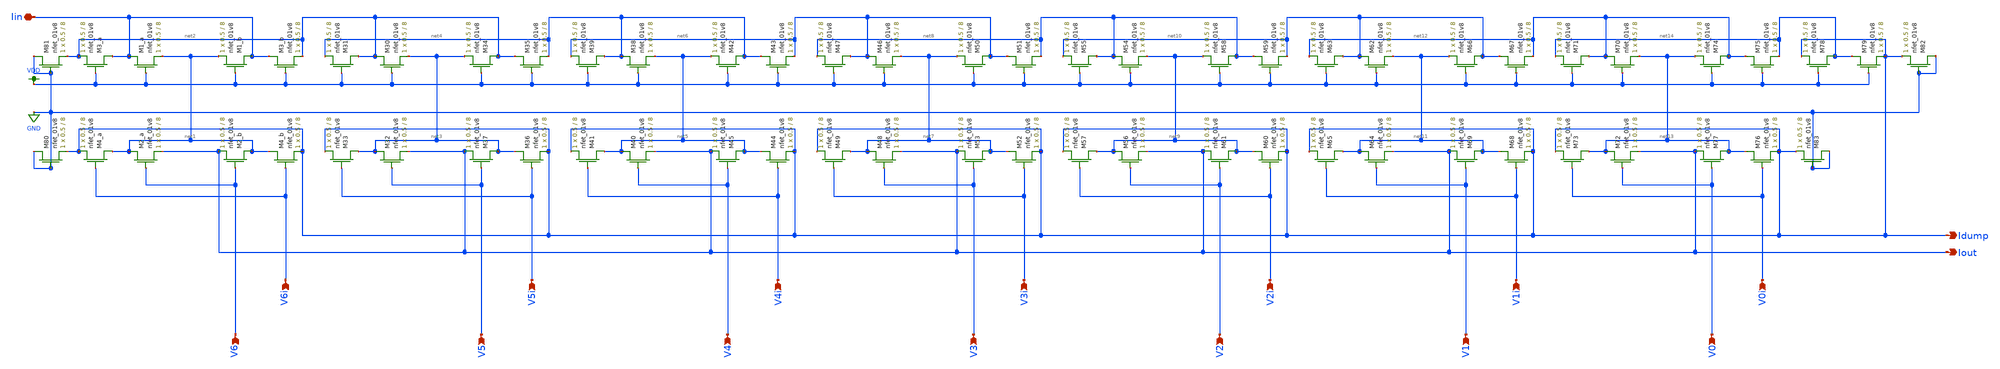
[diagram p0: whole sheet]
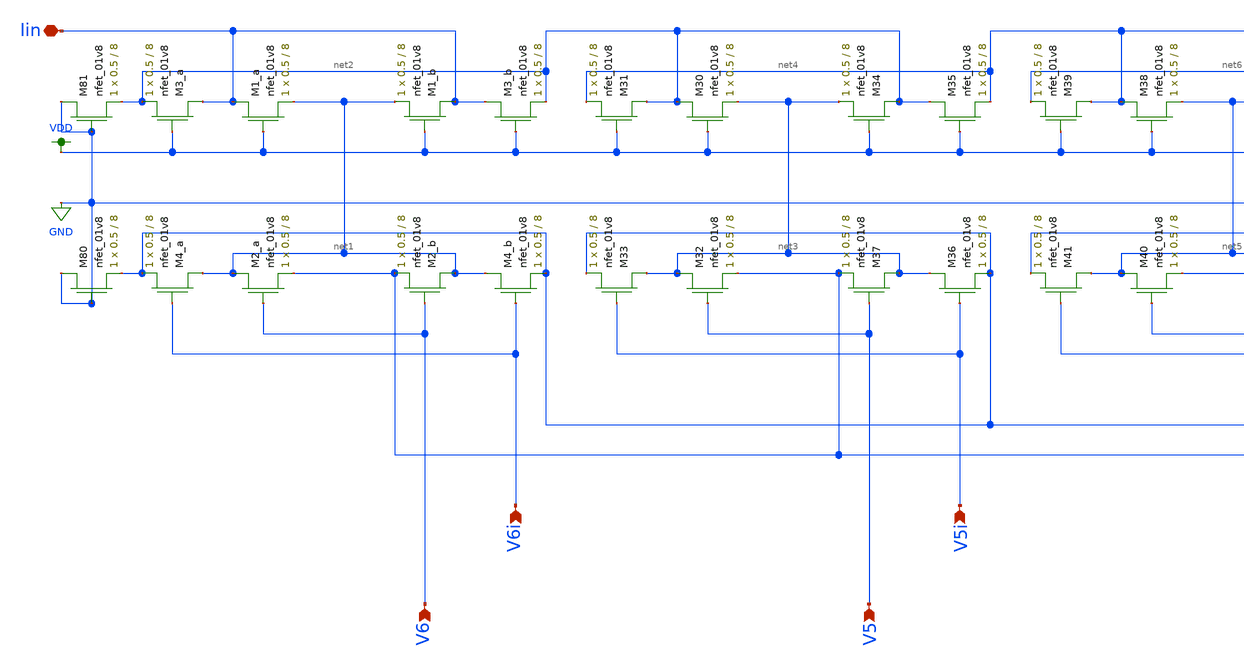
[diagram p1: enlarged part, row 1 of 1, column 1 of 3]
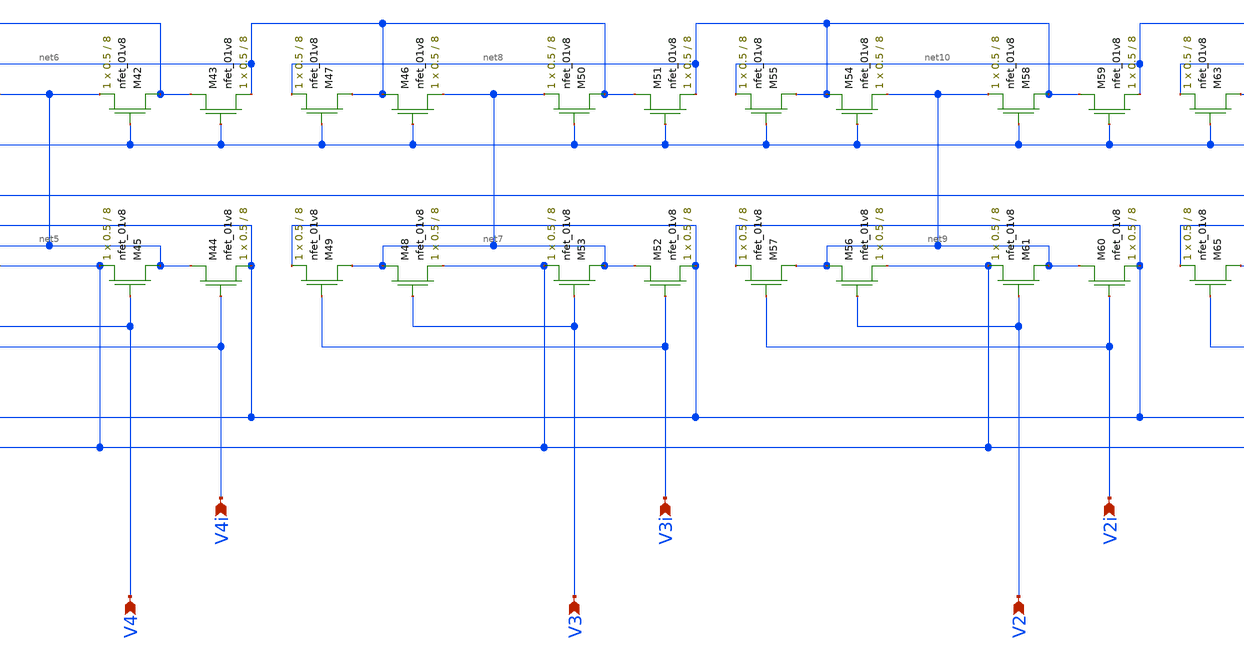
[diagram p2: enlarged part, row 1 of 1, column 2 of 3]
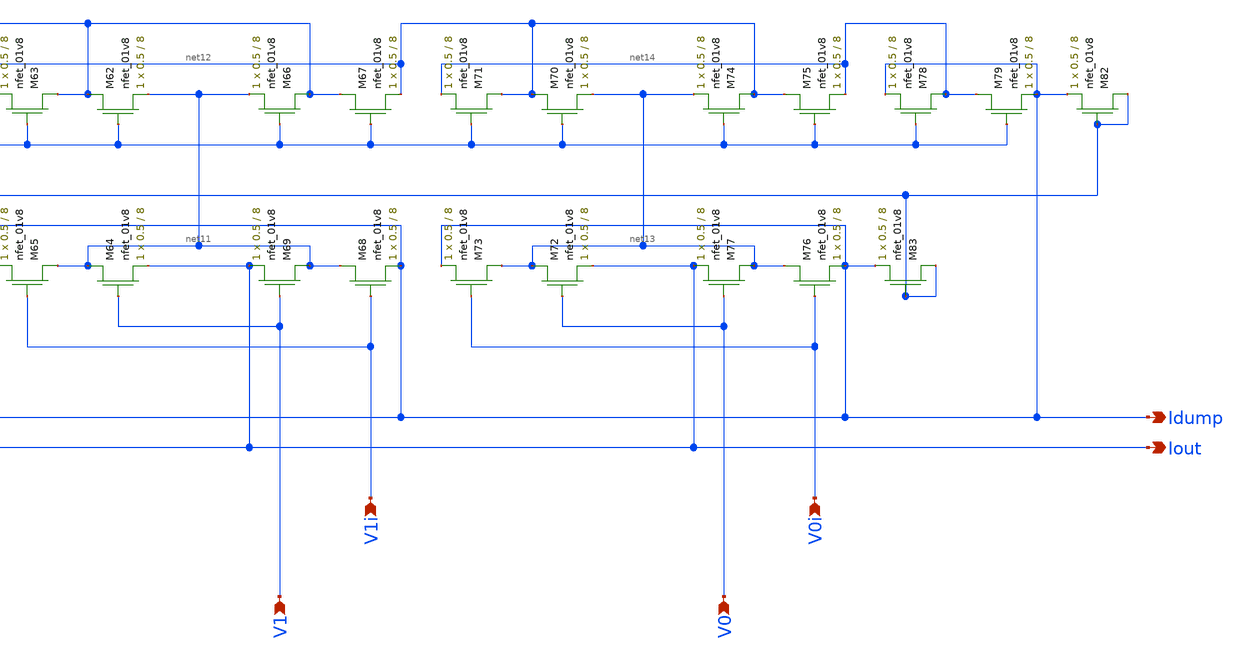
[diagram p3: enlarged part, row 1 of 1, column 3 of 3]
** sch_path: xschem/old_files/ladder.sch
**.subckt ladder Iin Idump Iout V6 V5 V4 V3 V2 V1 V0 V6i V5i V4i V3i V2i V1i V0i
*.iopin Iin
*.opin Idump
*.opin Iout
*.ipin V6
*.ipin V5
*.ipin V4
*.ipin V3
*.ipin V2
*.ipin V1
*.ipin V0
*.ipin V6i
*.ipin V5i
*.ipin V4i
*.ipin V3i
*.ipin V2i
*.ipin V1i
*.ipin V0i
XM1_a Iin VDD net1 GND sky130_fd_pr__nfet_01v8 L=8 W=0.5 nf=1 ad='int((nf+1)/2) * W/nf * 0.29' as='int((nf+2)/2) * W/nf * 0.29'
+ pd='2*int((nf+1)/2) * (W/nf + 0.29)' ps='2*int((nf+2)/2) * (W/nf + 0.29)' nrd='0.29 / W' nrs='0.29 / W'
+ sa=0 sb=0 sd=0 mult=1 m=1
XM3_a Iin VDD net2 GND sky130_fd_pr__nfet_01v8 L=8 W=0.5 nf=1 ad='int((nf+1)/2) * W/nf * 0.29' as='int((nf+2)/2) * W/nf * 0.29'
+ pd='2*int((nf+1)/2) * (W/nf + 0.29)' ps='2*int((nf+2)/2) * (W/nf + 0.29)' nrd='0.29 / W' nrs='0.29 / W'
+ sa=0 sb=0 sd=0 mult=1 m=1
XM2_a net1 V6 Iout GND sky130_fd_pr__nfet_01v8 L=8 W=0.5 nf=1 ad='int((nf+1)/2) * W/nf * 0.29' as='int((nf+2)/2) * W/nf * 0.29'
+ pd='2*int((nf+1)/2) * (W/nf + 0.29)' ps='2*int((nf+2)/2) * (W/nf + 0.29)' nrd='0.29 / W' nrs='0.29 / W'
+ sa=0 sb=0 sd=0 mult=1 m=1
XM4_a net1 V6i Idump GND sky130_fd_pr__nfet_01v8 L=8 W=0.5 nf=1 ad='int((nf+1)/2) * W/nf * 0.29' as='int((nf+2)/2) * W/nf * 0.29'
+ pd='2*int((nf+1)/2) * (W/nf + 0.29)' ps='2*int((nf+2)/2) * (W/nf + 0.29)' nrd='0.29 / W' nrs='0.29 / W'
+ sa=0 sb=0 sd=0 mult=1 m=1
XM1_b Iin VDD net1 GND sky130_fd_pr__nfet_01v8 L=8 W=0.5 nf=1 ad='int((nf+1)/2) * W/nf * 0.29' as='int((nf+2)/2) * W/nf * 0.29'
+ pd='2*int((nf+1)/2) * (W/nf + 0.29)' ps='2*int((nf+2)/2) * (W/nf + 0.29)' nrd='0.29 / W' nrs='0.29 / W'
+ sa=0 sb=0 sd=0 mult=1 m=1
XM3_b Iin VDD net2 GND sky130_fd_pr__nfet_01v8 L=8 W=0.5 nf=1 ad='int((nf+1)/2) * W/nf * 0.29' as='int((nf+2)/2) * W/nf * 0.29'
+ pd='2*int((nf+1)/2) * (W/nf + 0.29)' ps='2*int((nf+2)/2) * (W/nf + 0.29)' nrd='0.29 / W' nrs='0.29 / W'
+ sa=0 sb=0 sd=0 mult=1 m=1
XM4_b net1 V6i Idump GND sky130_fd_pr__nfet_01v8 L=8 W=0.5 nf=1 ad='int((nf+1)/2) * W/nf * 0.29' as='int((nf+2)/2) * W/nf * 0.29'
+ pd='2*int((nf+1)/2) * (W/nf + 0.29)' ps='2*int((nf+2)/2) * (W/nf + 0.29)' nrd='0.29 / W' nrs='0.29 / W'
+ sa=0 sb=0 sd=0 mult=1 m=1
XM2_b net1 V6 Iout GND sky130_fd_pr__nfet_01v8 L=8 W=0.5 nf=1 ad='int((nf+1)/2) * W/nf * 0.29' as='int((nf+2)/2) * W/nf * 0.29'
+ pd='2*int((nf+1)/2) * (W/nf + 0.29)' ps='2*int((nf+2)/2) * (W/nf + 0.29)' nrd='0.29 / W' nrs='0.29 / W'
+ sa=0 sb=0 sd=0 mult=1 m=1
XM30 net2 VDD net3 GND sky130_fd_pr__nfet_01v8 L=8 W=0.5 nf=1 ad='int((nf+1)/2) * W/nf * 0.29' as='int((nf+2)/2) * W/nf * 0.29'
+ pd='2*int((nf+1)/2) * (W/nf + 0.29)' ps='2*int((nf+2)/2) * (W/nf + 0.29)' nrd='0.29 / W' nrs='0.29 / W'
+ sa=0 sb=0 sd=0 mult=1 m=1
XM31 net2 VDD net4 GND sky130_fd_pr__nfet_01v8 L=8 W=0.5 nf=1 ad='int((nf+1)/2) * W/nf * 0.29' as='int((nf+2)/2) * W/nf * 0.29'
+ pd='2*int((nf+1)/2) * (W/nf + 0.29)' ps='2*int((nf+2)/2) * (W/nf + 0.29)' nrd='0.29 / W' nrs='0.29 / W'
+ sa=0 sb=0 sd=0 mult=1 m=1
XM32 net3 V5 Iout GND sky130_fd_pr__nfet_01v8 L=8 W=0.5 nf=1 ad='int((nf+1)/2) * W/nf * 0.29' as='int((nf+2)/2) * W/nf * 0.29'
+ pd='2*int((nf+1)/2) * (W/nf + 0.29)' ps='2*int((nf+2)/2) * (W/nf + 0.29)' nrd='0.29 / W' nrs='0.29 / W'
+ sa=0 sb=0 sd=0 mult=1 m=1
XM33 net3 V5i Idump GND sky130_fd_pr__nfet_01v8 L=8 W=0.5 nf=1 ad='int((nf+1)/2) * W/nf * 0.29' as='int((nf+2)/2) * W/nf * 0.29'
+ pd='2*int((nf+1)/2) * (W/nf + 0.29)' ps='2*int((nf+2)/2) * (W/nf + 0.29)' nrd='0.29 / W' nrs='0.29 / W'
+ sa=0 sb=0 sd=0 mult=1 m=1
XM34 net2 VDD net3 GND sky130_fd_pr__nfet_01v8 L=8 W=0.5 nf=1 ad='int((nf+1)/2) * W/nf * 0.29' as='int((nf+2)/2) * W/nf * 0.29'
+ pd='2*int((nf+1)/2) * (W/nf + 0.29)' ps='2*int((nf+2)/2) * (W/nf + 0.29)' nrd='0.29 / W' nrs='0.29 / W'
+ sa=0 sb=0 sd=0 mult=1 m=1
XM35 net2 VDD net4 GND sky130_fd_pr__nfet_01v8 L=8 W=0.5 nf=1 ad='int((nf+1)/2) * W/nf * 0.29' as='int((nf+2)/2) * W/nf * 0.29'
+ pd='2*int((nf+1)/2) * (W/nf + 0.29)' ps='2*int((nf+2)/2) * (W/nf + 0.29)' nrd='0.29 / W' nrs='0.29 / W'
+ sa=0 sb=0 sd=0 mult=1 m=1
XM36 net3 V5i Idump GND sky130_fd_pr__nfet_01v8 L=8 W=0.5 nf=1 ad='int((nf+1)/2) * W/nf * 0.29' as='int((nf+2)/2) * W/nf * 0.29'
+ pd='2*int((nf+1)/2) * (W/nf + 0.29)' ps='2*int((nf+2)/2) * (W/nf + 0.29)' nrd='0.29 / W' nrs='0.29 / W'
+ sa=0 sb=0 sd=0 mult=1 m=1
XM37 net3 V5 Iout GND sky130_fd_pr__nfet_01v8 L=8 W=0.5 nf=1 ad='int((nf+1)/2) * W/nf * 0.29' as='int((nf+2)/2) * W/nf * 0.29'
+ pd='2*int((nf+1)/2) * (W/nf + 0.29)' ps='2*int((nf+2)/2) * (W/nf + 0.29)' nrd='0.29 / W' nrs='0.29 / W'
+ sa=0 sb=0 sd=0 mult=1 m=1
XM38 net4 VDD net5 GND sky130_fd_pr__nfet_01v8 L=8 W=0.5 nf=1 ad='int((nf+1)/2) * W/nf * 0.29' as='int((nf+2)/2) * W/nf * 0.29'
+ pd='2*int((nf+1)/2) * (W/nf + 0.29)' ps='2*int((nf+2)/2) * (W/nf + 0.29)' nrd='0.29 / W' nrs='0.29 / W'
+ sa=0 sb=0 sd=0 mult=1 m=1
XM39 net4 VDD net6 GND sky130_fd_pr__nfet_01v8 L=8 W=0.5 nf=1 ad='int((nf+1)/2) * W/nf * 0.29' as='int((nf+2)/2) * W/nf * 0.29'
+ pd='2*int((nf+1)/2) * (W/nf + 0.29)' ps='2*int((nf+2)/2) * (W/nf + 0.29)' nrd='0.29 / W' nrs='0.29 / W'
+ sa=0 sb=0 sd=0 mult=1 m=1
XM40 net5 V4 Iout GND sky130_fd_pr__nfet_01v8 L=8 W=0.5 nf=1 ad='int((nf+1)/2) * W/nf * 0.29' as='int((nf+2)/2) * W/nf * 0.29'
+ pd='2*int((nf+1)/2) * (W/nf + 0.29)' ps='2*int((nf+2)/2) * (W/nf + 0.29)' nrd='0.29 / W' nrs='0.29 / W'
+ sa=0 sb=0 sd=0 mult=1 m=1
XM41 net5 V4i Idump GND sky130_fd_pr__nfet_01v8 L=8 W=0.5 nf=1 ad='int((nf+1)/2) * W/nf * 0.29' as='int((nf+2)/2) * W/nf * 0.29'
+ pd='2*int((nf+1)/2) * (W/nf + 0.29)' ps='2*int((nf+2)/2) * (W/nf + 0.29)' nrd='0.29 / W' nrs='0.29 / W'
+ sa=0 sb=0 sd=0 mult=1 m=1
XM42 net4 VDD net5 GND sky130_fd_pr__nfet_01v8 L=8 W=0.5 nf=1 ad='int((nf+1)/2) * W/nf * 0.29' as='int((nf+2)/2) * W/nf * 0.29'
+ pd='2*int((nf+1)/2) * (W/nf + 0.29)' ps='2*int((nf+2)/2) * (W/nf + 0.29)' nrd='0.29 / W' nrs='0.29 / W'
+ sa=0 sb=0 sd=0 mult=1 m=1
XM43 net4 VDD net6 GND sky130_fd_pr__nfet_01v8 L=8 W=0.5 nf=1 ad='int((nf+1)/2) * W/nf * 0.29' as='int((nf+2)/2) * W/nf * 0.29'
+ pd='2*int((nf+1)/2) * (W/nf + 0.29)' ps='2*int((nf+2)/2) * (W/nf + 0.29)' nrd='0.29 / W' nrs='0.29 / W'
+ sa=0 sb=0 sd=0 mult=1 m=1
XM44 net5 V4i Idump GND sky130_fd_pr__nfet_01v8 L=8 W=0.5 nf=1 ad='int((nf+1)/2) * W/nf * 0.29' as='int((nf+2)/2) * W/nf * 0.29'
+ pd='2*int((nf+1)/2) * (W/nf + 0.29)' ps='2*int((nf+2)/2) * (W/nf + 0.29)' nrd='0.29 / W' nrs='0.29 / W'
+ sa=0 sb=0 sd=0 mult=1 m=1
XM45 net5 V4 Iout GND sky130_fd_pr__nfet_01v8 L=8 W=0.5 nf=1 ad='int((nf+1)/2) * W/nf * 0.29' as='int((nf+2)/2) * W/nf * 0.29'
+ pd='2*int((nf+1)/2) * (W/nf + 0.29)' ps='2*int((nf+2)/2) * (W/nf + 0.29)' nrd='0.29 / W' nrs='0.29 / W'
+ sa=0 sb=0 sd=0 mult=1 m=1
XM46 net6 VDD net7 GND sky130_fd_pr__nfet_01v8 L=8 W=0.5 nf=1 ad='int((nf+1)/2) * W/nf * 0.29' as='int((nf+2)/2) * W/nf * 0.29'
+ pd='2*int((nf+1)/2) * (W/nf + 0.29)' ps='2*int((nf+2)/2) * (W/nf + 0.29)' nrd='0.29 / W' nrs='0.29 / W'
+ sa=0 sb=0 sd=0 mult=1 m=1
XM47 net6 VDD net8 GND sky130_fd_pr__nfet_01v8 L=8 W=0.5 nf=1 ad='int((nf+1)/2) * W/nf * 0.29' as='int((nf+2)/2) * W/nf * 0.29'
+ pd='2*int((nf+1)/2) * (W/nf + 0.29)' ps='2*int((nf+2)/2) * (W/nf + 0.29)' nrd='0.29 / W' nrs='0.29 / W'
+ sa=0 sb=0 sd=0 mult=1 m=1
XM48 net7 V3 Iout GND sky130_fd_pr__nfet_01v8 L=8 W=0.5 nf=1 ad='int((nf+1)/2) * W/nf * 0.29' as='int((nf+2)/2) * W/nf * 0.29'
+ pd='2*int((nf+1)/2) * (W/nf + 0.29)' ps='2*int((nf+2)/2) * (W/nf + 0.29)' nrd='0.29 / W' nrs='0.29 / W'
+ sa=0 sb=0 sd=0 mult=1 m=1
XM49 net7 V3i Idump GND sky130_fd_pr__nfet_01v8 L=8 W=0.5 nf=1 ad='int((nf+1)/2) * W/nf * 0.29' as='int((nf+2)/2) * W/nf * 0.29'
+ pd='2*int((nf+1)/2) * (W/nf + 0.29)' ps='2*int((nf+2)/2) * (W/nf + 0.29)' nrd='0.29 / W' nrs='0.29 / W'
+ sa=0 sb=0 sd=0 mult=1 m=1
XM50 net6 VDD net7 GND sky130_fd_pr__nfet_01v8 L=8 W=0.5 nf=1 ad='int((nf+1)/2) * W/nf * 0.29' as='int((nf+2)/2) * W/nf * 0.29'
+ pd='2*int((nf+1)/2) * (W/nf + 0.29)' ps='2*int((nf+2)/2) * (W/nf + 0.29)' nrd='0.29 / W' nrs='0.29 / W'
+ sa=0 sb=0 sd=0 mult=1 m=1
XM51 net6 VDD net8 GND sky130_fd_pr__nfet_01v8 L=8 W=0.5 nf=1 ad='int((nf+1)/2) * W/nf * 0.29' as='int((nf+2)/2) * W/nf * 0.29'
+ pd='2*int((nf+1)/2) * (W/nf + 0.29)' ps='2*int((nf+2)/2) * (W/nf + 0.29)' nrd='0.29 / W' nrs='0.29 / W'
+ sa=0 sb=0 sd=0 mult=1 m=1
XM52 net7 V3i Idump GND sky130_fd_pr__nfet_01v8 L=8 W=0.5 nf=1 ad='int((nf+1)/2) * W/nf * 0.29' as='int((nf+2)/2) * W/nf * 0.29'
+ pd='2*int((nf+1)/2) * (W/nf + 0.29)' ps='2*int((nf+2)/2) * (W/nf + 0.29)' nrd='0.29 / W' nrs='0.29 / W'
+ sa=0 sb=0 sd=0 mult=1 m=1
XM53 net7 V3 Iout GND sky130_fd_pr__nfet_01v8 L=8 W=0.5 nf=1 ad='int((nf+1)/2) * W/nf * 0.29' as='int((nf+2)/2) * W/nf * 0.29'
+ pd='2*int((nf+1)/2) * (W/nf + 0.29)' ps='2*int((nf+2)/2) * (W/nf + 0.29)' nrd='0.29 / W' nrs='0.29 / W'
+ sa=0 sb=0 sd=0 mult=1 m=1
XM54 net8 VDD net9 GND sky130_fd_pr__nfet_01v8 L=8 W=0.5 nf=1 ad='int((nf+1)/2) * W/nf * 0.29' as='int((nf+2)/2) * W/nf * 0.29'
+ pd='2*int((nf+1)/2) * (W/nf + 0.29)' ps='2*int((nf+2)/2) * (W/nf + 0.29)' nrd='0.29 / W' nrs='0.29 / W'
+ sa=0 sb=0 sd=0 mult=1 m=1
XM55 net8 VDD net10 GND sky130_fd_pr__nfet_01v8 L=8 W=0.5 nf=1 ad='int((nf+1)/2) * W/nf * 0.29' as='int((nf+2)/2) * W/nf * 0.29'
+ pd='2*int((nf+1)/2) * (W/nf + 0.29)' ps='2*int((nf+2)/2) * (W/nf + 0.29)' nrd='0.29 / W' nrs='0.29 / W'
+ sa=0 sb=0 sd=0 mult=1 m=1
XM56 net9 V2 Iout GND sky130_fd_pr__nfet_01v8 L=8 W=0.5 nf=1 ad='int((nf+1)/2) * W/nf * 0.29' as='int((nf+2)/2) * W/nf * 0.29'
+ pd='2*int((nf+1)/2) * (W/nf + 0.29)' ps='2*int((nf+2)/2) * (W/nf + 0.29)' nrd='0.29 / W' nrs='0.29 / W'
+ sa=0 sb=0 sd=0 mult=1 m=1
XM57 net9 V2i Idump GND sky130_fd_pr__nfet_01v8 L=8 W=0.5 nf=1 ad='int((nf+1)/2) * W/nf * 0.29' as='int((nf+2)/2) * W/nf * 0.29'
+ pd='2*int((nf+1)/2) * (W/nf + 0.29)' ps='2*int((nf+2)/2) * (W/nf + 0.29)' nrd='0.29 / W' nrs='0.29 / W'
+ sa=0 sb=0 sd=0 mult=1 m=1
XM58 net8 VDD net9 GND sky130_fd_pr__nfet_01v8 L=8 W=0.5 nf=1 ad='int((nf+1)/2) * W/nf * 0.29' as='int((nf+2)/2) * W/nf * 0.29'
+ pd='2*int((nf+1)/2) * (W/nf + 0.29)' ps='2*int((nf+2)/2) * (W/nf + 0.29)' nrd='0.29 / W' nrs='0.29 / W'
+ sa=0 sb=0 sd=0 mult=1 m=1
XM59 net8 VDD net10 GND sky130_fd_pr__nfet_01v8 L=8 W=0.5 nf=1 ad='int((nf+1)/2) * W/nf * 0.29' as='int((nf+2)/2) * W/nf * 0.29'
+ pd='2*int((nf+1)/2) * (W/nf + 0.29)' ps='2*int((nf+2)/2) * (W/nf + 0.29)' nrd='0.29 / W' nrs='0.29 / W'
+ sa=0 sb=0 sd=0 mult=1 m=1
XM60 net9 V2i Idump GND sky130_fd_pr__nfet_01v8 L=8 W=0.5 nf=1 ad='int((nf+1)/2) * W/nf * 0.29' as='int((nf+2)/2) * W/nf * 0.29'
+ pd='2*int((nf+1)/2) * (W/nf + 0.29)' ps='2*int((nf+2)/2) * (W/nf + 0.29)' nrd='0.29 / W' nrs='0.29 / W'
+ sa=0 sb=0 sd=0 mult=1 m=1
XM61 net9 V2 Iout GND sky130_fd_pr__nfet_01v8 L=8 W=0.5 nf=1 ad='int((nf+1)/2) * W/nf * 0.29' as='int((nf+2)/2) * W/nf * 0.29'
+ pd='2*int((nf+1)/2) * (W/nf + 0.29)' ps='2*int((nf+2)/2) * (W/nf + 0.29)' nrd='0.29 / W' nrs='0.29 / W'
+ sa=0 sb=0 sd=0 mult=1 m=1
XM62 net10 VDD net11 GND sky130_fd_pr__nfet_01v8 L=8 W=0.5 nf=1 ad='int((nf+1)/2) * W/nf * 0.29' as='int((nf+2)/2) * W/nf * 0.29'
+ pd='2*int((nf+1)/2) * (W/nf + 0.29)' ps='2*int((nf+2)/2) * (W/nf + 0.29)' nrd='0.29 / W' nrs='0.29 / W'
+ sa=0 sb=0 sd=0 mult=1 m=1
XM63 net10 VDD net12 GND sky130_fd_pr__nfet_01v8 L=8 W=0.5 nf=1 ad='int((nf+1)/2) * W/nf * 0.29' as='int((nf+2)/2) * W/nf * 0.29'
+ pd='2*int((nf+1)/2) * (W/nf + 0.29)' ps='2*int((nf+2)/2) * (W/nf + 0.29)' nrd='0.29 / W' nrs='0.29 / W'
+ sa=0 sb=0 sd=0 mult=1 m=1
XM64 net11 V1 Iout GND sky130_fd_pr__nfet_01v8 L=8 W=0.5 nf=1 ad='int((nf+1)/2) * W/nf * 0.29' as='int((nf+2)/2) * W/nf * 0.29'
+ pd='2*int((nf+1)/2) * (W/nf + 0.29)' ps='2*int((nf+2)/2) * (W/nf + 0.29)' nrd='0.29 / W' nrs='0.29 / W'
+ sa=0 sb=0 sd=0 mult=1 m=1
XM65 net11 V1i Idump GND sky130_fd_pr__nfet_01v8 L=8 W=0.5 nf=1 ad='int((nf+1)/2) * W/nf * 0.29' as='int((nf+2)/2) * W/nf * 0.29'
+ pd='2*int((nf+1)/2) * (W/nf + 0.29)' ps='2*int((nf+2)/2) * (W/nf + 0.29)' nrd='0.29 / W' nrs='0.29 / W'
+ sa=0 sb=0 sd=0 mult=1 m=1
XM66 net10 VDD net11 GND sky130_fd_pr__nfet_01v8 L=8 W=0.5 nf=1 ad='int((nf+1)/2) * W/nf * 0.29' as='int((nf+2)/2) * W/nf * 0.29'
+ pd='2*int((nf+1)/2) * (W/nf + 0.29)' ps='2*int((nf+2)/2) * (W/nf + 0.29)' nrd='0.29 / W' nrs='0.29 / W'
+ sa=0 sb=0 sd=0 mult=1 m=1
XM67 net10 VDD net12 GND sky130_fd_pr__nfet_01v8 L=8 W=0.5 nf=1 ad='int((nf+1)/2) * W/nf * 0.29' as='int((nf+2)/2) * W/nf * 0.29'
+ pd='2*int((nf+1)/2) * (W/nf + 0.29)' ps='2*int((nf+2)/2) * (W/nf + 0.29)' nrd='0.29 / W' nrs='0.29 / W'
+ sa=0 sb=0 sd=0 mult=1 m=1
XM68 net11 V1i Idump GND sky130_fd_pr__nfet_01v8 L=8 W=0.5 nf=1 ad='int((nf+1)/2) * W/nf * 0.29' as='int((nf+2)/2) * W/nf * 0.29'
+ pd='2*int((nf+1)/2) * (W/nf + 0.29)' ps='2*int((nf+2)/2) * (W/nf + 0.29)' nrd='0.29 / W' nrs='0.29 / W'
+ sa=0 sb=0 sd=0 mult=1 m=1
XM69 net11 V1 Iout GND sky130_fd_pr__nfet_01v8 L=8 W=0.5 nf=1 ad='int((nf+1)/2) * W/nf * 0.29' as='int((nf+2)/2) * W/nf * 0.29'
+ pd='2*int((nf+1)/2) * (W/nf + 0.29)' ps='2*int((nf+2)/2) * (W/nf + 0.29)' nrd='0.29 / W' nrs='0.29 / W'
+ sa=0 sb=0 sd=0 mult=1 m=1
XM70 net12 VDD net13 GND sky130_fd_pr__nfet_01v8 L=8 W=0.5 nf=1 ad='int((nf+1)/2) * W/nf * 0.29' as='int((nf+2)/2) * W/nf * 0.29'
+ pd='2*int((nf+1)/2) * (W/nf + 0.29)' ps='2*int((nf+2)/2) * (W/nf + 0.29)' nrd='0.29 / W' nrs='0.29 / W'
+ sa=0 sb=0 sd=0 mult=1 m=1
XM71 net12 VDD net14 GND sky130_fd_pr__nfet_01v8 L=8 W=0.5 nf=1 ad='int((nf+1)/2) * W/nf * 0.29' as='int((nf+2)/2) * W/nf * 0.29'
+ pd='2*int((nf+1)/2) * (W/nf + 0.29)' ps='2*int((nf+2)/2) * (W/nf + 0.29)' nrd='0.29 / W' nrs='0.29 / W'
+ sa=0 sb=0 sd=0 mult=1 m=1
XM72 net13 V0 Iout GND sky130_fd_pr__nfet_01v8 L=8 W=0.5 nf=1 ad='int((nf+1)/2) * W/nf * 0.29' as='int((nf+2)/2) * W/nf * 0.29'
+ pd='2*int((nf+1)/2) * (W/nf + 0.29)' ps='2*int((nf+2)/2) * (W/nf + 0.29)' nrd='0.29 / W' nrs='0.29 / W'
+ sa=0 sb=0 sd=0 mult=1 m=1
XM73 net13 V0i Idump GND sky130_fd_pr__nfet_01v8 L=8 W=0.5 nf=1 ad='int((nf+1)/2) * W/nf * 0.29' as='int((nf+2)/2) * W/nf * 0.29'
+ pd='2*int((nf+1)/2) * (W/nf + 0.29)' ps='2*int((nf+2)/2) * (W/nf + 0.29)' nrd='0.29 / W' nrs='0.29 / W'
+ sa=0 sb=0 sd=0 mult=1 m=1
XM74 net12 VDD net13 GND sky130_fd_pr__nfet_01v8 L=8 W=0.5 nf=1 ad='int((nf+1)/2) * W/nf * 0.29' as='int((nf+2)/2) * W/nf * 0.29'
+ pd='2*int((nf+1)/2) * (W/nf + 0.29)' ps='2*int((nf+2)/2) * (W/nf + 0.29)' nrd='0.29 / W' nrs='0.29 / W'
+ sa=0 sb=0 sd=0 mult=1 m=1
XM75 net12 VDD net14 GND sky130_fd_pr__nfet_01v8 L=8 W=0.5 nf=1 ad='int((nf+1)/2) * W/nf * 0.29' as='int((nf+2)/2) * W/nf * 0.29'
+ pd='2*int((nf+1)/2) * (W/nf + 0.29)' ps='2*int((nf+2)/2) * (W/nf + 0.29)' nrd='0.29 / W' nrs='0.29 / W'
+ sa=0 sb=0 sd=0 mult=1 m=1
XM76 net13 V0i Idump GND sky130_fd_pr__nfet_01v8 L=8 W=0.5 nf=1 ad='int((nf+1)/2) * W/nf * 0.29' as='int((nf+2)/2) * W/nf * 0.29'
+ pd='2*int((nf+1)/2) * (W/nf + 0.29)' ps='2*int((nf+2)/2) * (W/nf + 0.29)' nrd='0.29 / W' nrs='0.29 / W'
+ sa=0 sb=0 sd=0 mult=1 m=1
XM77 net13 V0 Iout GND sky130_fd_pr__nfet_01v8 L=8 W=0.5 nf=1 ad='int((nf+1)/2) * W/nf * 0.29' as='int((nf+2)/2) * W/nf * 0.29'
+ pd='2*int((nf+1)/2) * (W/nf + 0.29)' ps='2*int((nf+2)/2) * (W/nf + 0.29)' nrd='0.29 / W' nrs='0.29 / W'
+ sa=0 sb=0 sd=0 mult=1 m=1
XM78 net14 VDD Idump GND sky130_fd_pr__nfet_01v8 L=8 W=0.5 nf=1 ad='int((nf+1)/2) * W/nf * 0.29' as='int((nf+2)/2) * W/nf * 0.29'
+ pd='2*int((nf+1)/2) * (W/nf + 0.29)' ps='2*int((nf+2)/2) * (W/nf + 0.29)' nrd='0.29 / W' nrs='0.29 / W'
+ sa=0 sb=0 sd=0 mult=1 m=1
XM79 net14 VDD Idump GND sky130_fd_pr__nfet_01v8 L=8 W=0.5 nf=1 ad='int((nf+1)/2) * W/nf * 0.29' as='int((nf+2)/2) * W/nf * 0.29'
+ pd='2*int((nf+1)/2) * (W/nf + 0.29)' ps='2*int((nf+2)/2) * (W/nf + 0.29)' nrd='0.29 / W' nrs='0.29 / W'
+ sa=0 sb=0 sd=0 mult=1 m=1
XM80 GND GND Idump GND sky130_fd_pr__nfet_01v8 L=8 W=0.5 nf=1 ad='int((nf+1)/2) * W/nf * 0.29' as='int((nf+2)/2) * W/nf * 0.29'
+ pd='2*int((nf+1)/2) * (W/nf + 0.29)' ps='2*int((nf+2)/2) * (W/nf + 0.29)' nrd='0.29 / W' nrs='0.29 / W'
+ sa=0 sb=0 sd=0 mult=1 m=1
XM81 GND GND net2 GND sky130_fd_pr__nfet_01v8 L=8 W=0.5 nf=1 ad='int((nf+1)/2) * W/nf * 0.29' as='int((nf+2)/2) * W/nf * 0.29'
+ pd='2*int((nf+1)/2) * (W/nf + 0.29)' ps='2*int((nf+2)/2) * (W/nf + 0.29)' nrd='0.29 / W' nrs='0.29 / W'
+ sa=0 sb=0 sd=0 mult=1 m=1
XM82 GND GND Idump GND sky130_fd_pr__nfet_01v8 L=8 W=0.5 nf=1 ad='int((nf+1)/2) * W/nf * 0.29' as='int((nf+2)/2) * W/nf * 0.29'
+ pd='2*int((nf+1)/2) * (W/nf + 0.29)' ps='2*int((nf+2)/2) * (W/nf + 0.29)' nrd='0.29 / W' nrs='0.29 / W'
+ sa=0 sb=0 sd=0 mult=1 m=1
XM83 GND GND Idump GND sky130_fd_pr__nfet_01v8 L=8 W=0.5 nf=1 ad='int((nf+1)/2) * W/nf * 0.29' as='int((nf+2)/2) * W/nf * 0.29'
+ pd='2*int((nf+1)/2) * (W/nf + 0.29)' ps='2*int((nf+2)/2) * (W/nf + 0.29)' nrd='0.29 / W' nrs='0.29 / W'
+ sa=0 sb=0 sd=0 mult=1 m=1
**.ends
.GLOBAL VDD
.GLOBAL GND
.end
